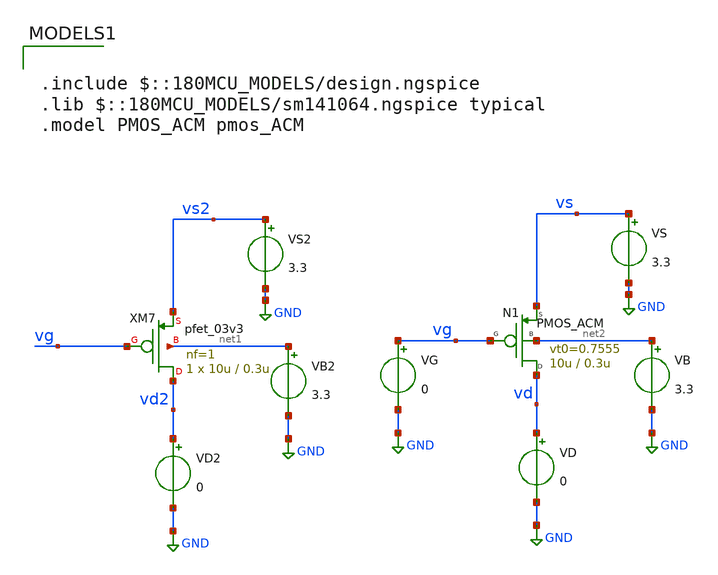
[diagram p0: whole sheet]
** sch_path: legacy/Examples/GF180MCU/xschem/Extraction/TB_pmos_acm.sch
**.subckt TB_pmos_acm
VG vg GND 0
VS2 vs2 GND 3.3
VB2 net1 GND 3.3
VD2 vd2 GND 0
XM7 vd2 vg vs2 net1 pfet_03v3 L=0.3u W=10u nf=1 ad='int((nf+1)/2) * W/nf * 0.18u' as='int((nf+2)/2) * W/nf * 0.18u'
+ pd='2*int((nf+1)/2) * (W/nf + 0.18u)' ps='2*int((nf+2)/2) * (W/nf + 0.18u)' nrd='0.18u / W' nrs='0.18u / W'
+ sa=0 sb=0 sd=0 m=1
VS vs GND 3.3
VB net2 GND 3.3
VD vd GND 0
N1 vd vg vs net2 PMOS_ACM w=10u l=0.3u n=1.43 is=0.709u vt0=0.7555 sigma=18.8m zeta=6.7m
**** begin user architecture code

.include $::180MCU_MODELS/design.ngspice
.lib $::180MCU_MODELS/sm141064.ngspice typical
.model PMOS_ACM pmos_ACM



.control
pre_osdi ./PMOS_ACM_2V0.osdi
save all

dc VG -0.05 3.3 5m


*gm for ACM
let gm_id = -deriv(ln(i(Vd)))

*gm for GF180
let gm_id_gf = -deriv(ln(i(Vd2)))

save gm_id gm_id_gf
write TB_pmos_acm.raw

.endc


**** end user architecture code
**.ends
.GLOBAL GND
.end
